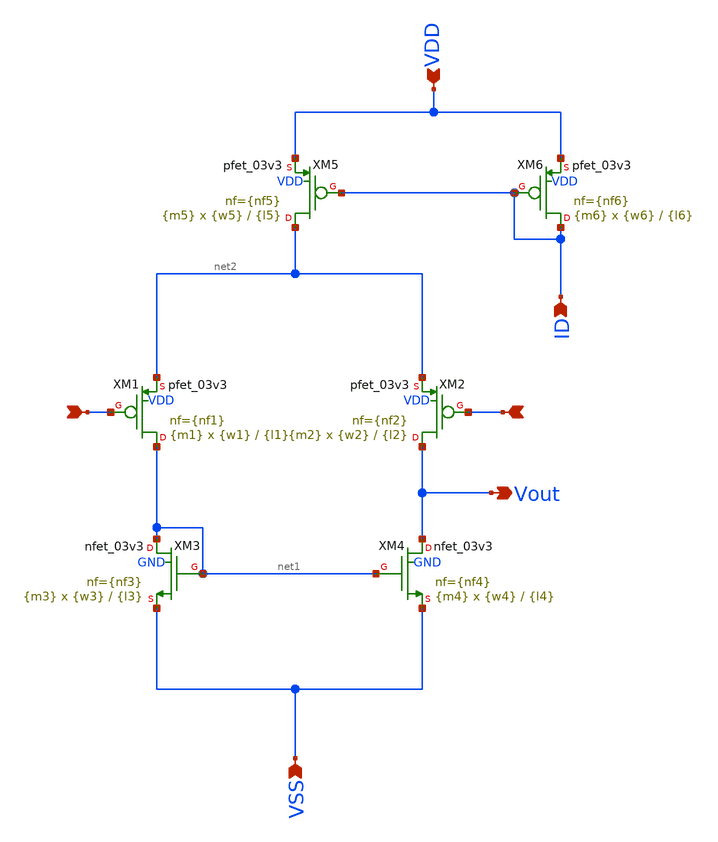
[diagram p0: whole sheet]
** sch_path: xschem/ota_miller/ota_p_in.sch
**.subckt ota_p_in Vout VSS VDD + - ID
*.opin Vout
*.ipin VSS
*.ipin VDD
*.ipin +
*.ipin -
*.ipin ID
XM1 net1 + net2 VDD pfet_03v3 L={l1} W={w1} nf={nf1} ad='int((nf+1)/2) * W/nf * 0.18u' as='int((nf+2)/2) * W/nf * 0.18u'
+ pd='2*int((nf+1)/2) * (W/nf + 0.18u)' ps='2*int((nf+2)/2) * (W/nf + 0.18u)' nrd='0.18u / W' nrs='0.18u / W'
+ sa=0 sb=0 sd=0 m={m1} par={m1}
XM2 Vout - net2 VDD pfet_03v3 L={l2} W={w2} nf={nf2} ad='int((nf+1)/2) * W/nf * 0.18u' as='int((nf+2)/2) * W/nf * 0.18u'
+ pd='2*int((nf+1)/2) * (W/nf + 0.18u)' ps='2*int((nf+2)/2) * (W/nf + 0.18u)' nrd='0.18u / W' nrs='0.18u / W'
+ sa=0 sb=0 sd=0 m={m2} par={m2}
XM3 net1 net1 VSS GND nfet_03v3 L={l3} W={w3} nf={nf3} ad='int((nf+1)/2) * W/nf * 0.18u' as='int((nf+2)/2) * W/nf * 0.18u'
+ pd='2*int((nf+1)/2) * (W/nf + 0.18u)' ps='2*int((nf+2)/2) * (W/nf + 0.18u)' nrd='0.18u / W' nrs='0.18u / W'
+ sa=0 sb=0 sd=0 m={m3} par={m3}
XM4 Vout net1 VSS GND nfet_03v3 L={l4} W={w4} nf={nf4} ad='int((nf+1)/2) * W/nf * 0.18u' as='int((nf+2)/2) * W/nf * 0.18u'
+ pd='2*int((nf+1)/2) * (W/nf + 0.18u)' ps='2*int((nf+2)/2) * (W/nf + 0.18u)' nrd='0.18u / W' nrs='0.18u / W'
+ sa=0 sb=0 sd=0 m={m4} par={m4}
XM5 net2 ID VDD VDD pfet_03v3 L={l5} W={w5} nf={nf5} ad='int((nf+1)/2) * W/nf * 0.18u' as='int((nf+2)/2) * W/nf * 0.18u'
+ pd='2*int((nf+1)/2) * (W/nf + 0.18u)' ps='2*int((nf+2)/2) * (W/nf + 0.18u)' nrd='0.18u / W' nrs='0.18u / W'
+ sa=0 sb=0 sd=0 m={m5} par={m5}
XM6 ID ID VDD VDD pfet_03v3 L={l6} W={w6} nf={nf6} ad='int((nf+1)/2) * W/nf * 0.18u' as='int((nf+2)/2) * W/nf * 0.18u'
+ pd='2*int((nf+1)/2) * (W/nf + 0.18u)' ps='2*int((nf+2)/2) * (W/nf + 0.18u)' nrd='0.18u / W' nrs='0.18u / W'
+ sa=0 sb=0 sd=0 m={m6} par={m6}
**** begin user architecture code


.param w1=29u l1=1u m1=1 nf1=1
.param w2=29u l2=1u m2=1 nf2=1
.param w3=0.22u l3=1.6u m3=1 nf3=1
.param w4=0.22u l4=1.6u m4=1 nf4=1
.param w5=1u l5=1u m5=4 nf5=1
.param w6=1u l6=1u m6=1 nf6=1




.include /home/ringosinye/eda/pdks/gf180mcuD/libs.tech/ngspice/design.ngspice
.lib /home/ringosinye/eda/pdks/gf180mcuD/libs.tech/ngspice/sm141064.ngspice typical


**** end user architecture code
**.ends
.end
